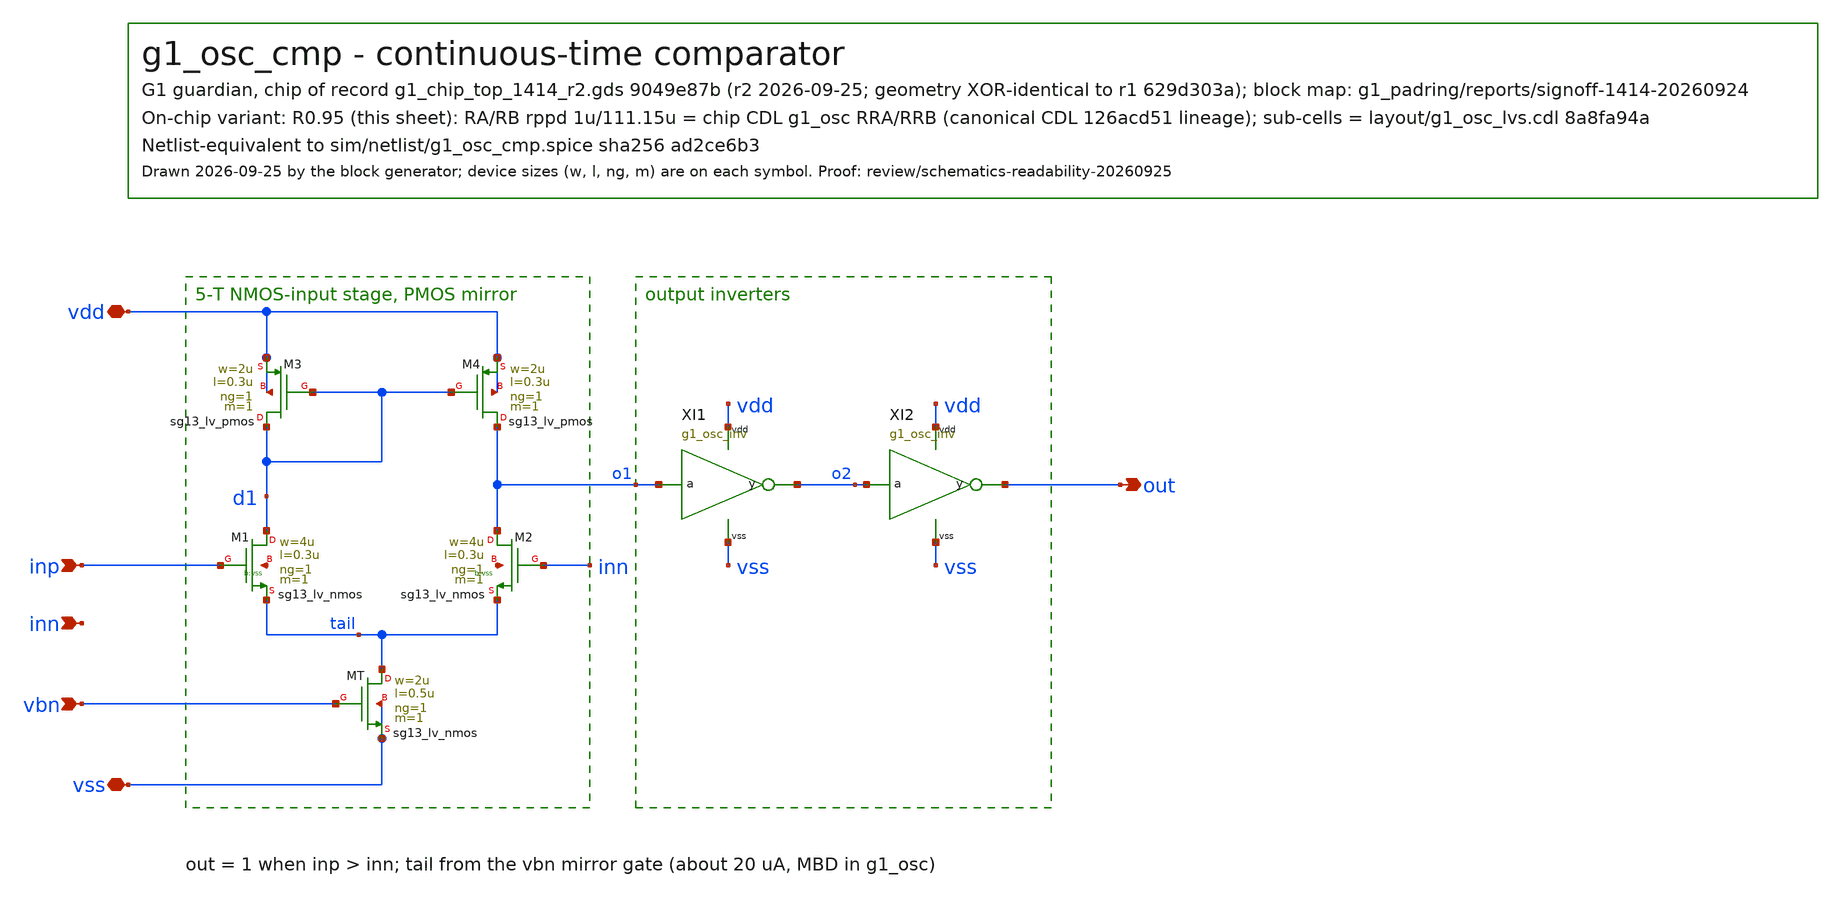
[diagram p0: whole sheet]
** sch_path: designs/g1-guardian/blocks/g1_osc/schematic/g1_osc_cmp.sch
**.subckt g1_osc_cmp inp inn vbn out vdd vss
*.ipin inp
*.ipin inn
*.ipin vbn
*.opin out
*.iopin vdd
*.iopin vss
XMT tail vbn vss vss sg13_lv_nmos w=2u l=0.5u ng=1 m=1 mm_ok=1
XM1 d1 inp tail vss sg13_lv_nmos w=4u l=0.3u ng=1 m=1 mm_ok=1
XM2 o1 inn tail vss sg13_lv_nmos w=4u l=0.3u ng=1 m=1 mm_ok=1
XM3 d1 d1 vdd vdd sg13_lv_pmos w=2u l=0.3u ng=1 m=1 mm_ok=1
XM4 o1 d1 vdd vdd sg13_lv_pmos w=2u l=0.3u ng=1 m=1 mm_ok=1
XI1 o1 o2 vdd vss g1_osc_inv
XI2 o2 out vdd vss g1_osc_inv
**.ends

* expanding   symbol:  g1_osc_inv.sym # of pins=4
** sym_path: designs/g1-guardian/blocks/g1_osc/schematic/g1_osc_inv.sym
** sch_path: designs/g1-guardian/blocks/g1_osc/schematic/g1_osc_inv.sch
.subckt g1_osc_inv a y vdd vss
*.ipin a
*.opin y
*.iopin vdd
*.iopin vss
XMP y a vdd vdd sg13_lv_pmos w=1u l=0.13u ng=1 m=1 mm_ok=1
XMN y a vss vss sg13_lv_nmos w=0.5u l=0.13u ng=1 m=1 mm_ok=1
.ends

.end
